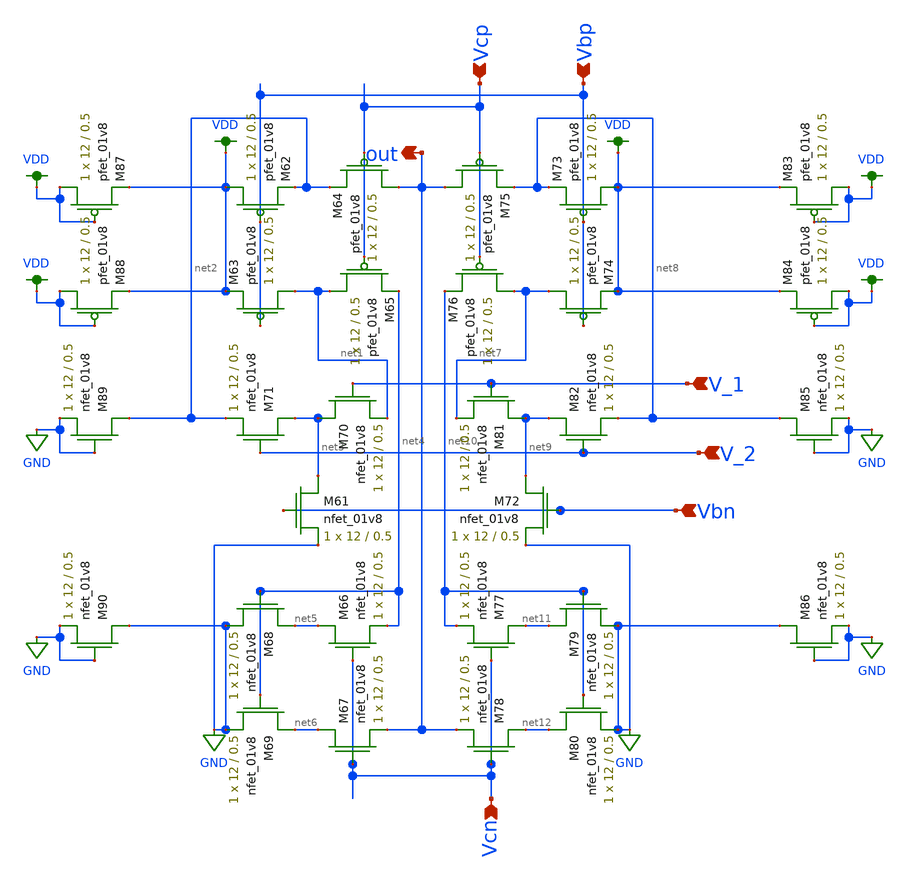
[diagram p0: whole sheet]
** sch_path: miniproject3/lfs.sch
**.subckt lfs V_1 Vcp Vcn Vbp Vbn V_2 out
*.ipin V_1
*.ipin Vcp
*.ipin Vcn
*.ipin Vbp
*.ipin Vbn
*.ipin V_2
*.opin out
XM61 net3 Vbn GND GND sky130_fd_pr__nfet_01v8 L=0.5 W=12 nf=1 ad='int((nf+1)/2) * W/nf * 0.29' as='int((nf+2)/2) * W/nf * 0.29'
+ pd='2*int((nf+1)/2) * (W/nf + 0.29)' ps='2*int((nf+2)/2) * (W/nf + 0.29)' nrd='0.29 / W' nrs='0.29 / W'
+ sa=0 sb=0 sd=0 mult=1 m=1
XM62 VDD Vbp net2 VDD sky130_fd_pr__pfet_01v8 L=0.5 W=12 nf=1 ad='int((nf+1)/2) * W/nf * 0.29' as='int((nf+2)/2) * W/nf * 0.29'
+ pd='2*int((nf+1)/2) * (W/nf + 0.29)' ps='2*int((nf+2)/2) * (W/nf + 0.29)' nrd='0.29 / W' nrs='0.29 / W'
+ sa=0 sb=0 sd=0 mult=1 m=1
XM63 net1 Vbp VDD VDD sky130_fd_pr__pfet_01v8 L=0.5 W=12 nf=1 ad='int((nf+1)/2) * W/nf * 0.29' as='int((nf+2)/2) * W/nf * 0.29'
+ pd='2*int((nf+1)/2) * (W/nf + 0.29)' ps='2*int((nf+2)/2) * (W/nf + 0.29)' nrd='0.29 / W' nrs='0.29 / W'
+ sa=0 sb=0 sd=0 mult=1 m=1
XM64 out Vcp net2 VDD sky130_fd_pr__pfet_01v8 L=0.5 W=12 nf=1 ad='int((nf+1)/2) * W/nf * 0.29' as='int((nf+2)/2) * W/nf * 0.29'
+ pd='2*int((nf+1)/2) * (W/nf + 0.29)' ps='2*int((nf+2)/2) * (W/nf + 0.29)' nrd='0.29 / W' nrs='0.29 / W'
+ sa=0 sb=0 sd=0 mult=1 m=1
XM65 net1 Vcp net4 VDD sky130_fd_pr__pfet_01v8 L=0.5 W=12 nf=1 ad='int((nf+1)/2) * W/nf * 0.29' as='int((nf+2)/2) * W/nf * 0.29'
+ pd='2*int((nf+1)/2) * (W/nf + 0.29)' ps='2*int((nf+2)/2) * (W/nf + 0.29)' nrd='0.29 / W' nrs='0.29 / W'
+ sa=0 sb=0 sd=0 mult=1 m=1
XM66 net5 Vcn net4 GND sky130_fd_pr__nfet_01v8 L=0.5 W=12 nf=1 ad='int((nf+1)/2) * W/nf * 0.29' as='int((nf+2)/2) * W/nf * 0.29'
+ pd='2*int((nf+1)/2) * (W/nf + 0.29)' ps='2*int((nf+2)/2) * (W/nf + 0.29)' nrd='0.29 / W' nrs='0.29 / W'
+ sa=0 sb=0 sd=0 mult=1 m=1
XM67 net6 Vcn out GND sky130_fd_pr__nfet_01v8 L=0.5 W=12 nf=1 ad='int((nf+1)/2) * W/nf * 0.29' as='int((nf+2)/2) * W/nf * 0.29'
+ pd='2*int((nf+1)/2) * (W/nf + 0.29)' ps='2*int((nf+2)/2) * (W/nf + 0.29)' nrd='0.29 / W' nrs='0.29 / W'
+ sa=0 sb=0 sd=0 mult=1 m=1
XM68 net5 net4 GND GND sky130_fd_pr__nfet_01v8 L=0.5 W=12 nf=1 ad='int((nf+1)/2) * W/nf * 0.29' as='int((nf+2)/2) * W/nf * 0.29'
+ pd='2*int((nf+1)/2) * (W/nf + 0.29)' ps='2*int((nf+2)/2) * (W/nf + 0.29)' nrd='0.29 / W' nrs='0.29 / W'
+ sa=0 sb=0 sd=0 mult=1 m=1
XM69 net6 net4 GND GND sky130_fd_pr__nfet_01v8 L=0.5 W=12 nf=1 ad='int((nf+1)/2) * W/nf * 0.29' as='int((nf+2)/2) * W/nf * 0.29'
+ pd='2*int((nf+1)/2) * (W/nf + 0.29)' ps='2*int((nf+2)/2) * (W/nf + 0.29)' nrd='0.29 / W' nrs='0.29 / W'
+ sa=0 sb=0 sd=0 mult=1 m=1
XM70 net3 V_1 net1 GND sky130_fd_pr__nfet_01v8 L=0.5 W=12 nf=1 ad='int((nf+1)/2) * W/nf * 0.29' as='int((nf+2)/2) * W/nf * 0.29'
+ pd='2*int((nf+1)/2) * (W/nf + 0.29)' ps='2*int((nf+2)/2) * (W/nf + 0.29)' nrd='0.29 / W' nrs='0.29 / W'
+ sa=0 sb=0 sd=0 mult=1 m=1
XM71 net3 V_2 net2 GND sky130_fd_pr__nfet_01v8 L=0.5 W=12 nf=1 ad='int((nf+1)/2) * W/nf * 0.29' as='int((nf+2)/2) * W/nf * 0.29'
+ pd='2*int((nf+1)/2) * (W/nf + 0.29)' ps='2*int((nf+2)/2) * (W/nf + 0.29)' nrd='0.29 / W' nrs='0.29 / W'
+ sa=0 sb=0 sd=0 mult=1 m=1
XM72 net9 Vbn GND GND sky130_fd_pr__nfet_01v8 L=0.5 W=12 nf=1 ad='int((nf+1)/2) * W/nf * 0.29' as='int((nf+2)/2) * W/nf * 0.29'
+ pd='2*int((nf+1)/2) * (W/nf + 0.29)' ps='2*int((nf+2)/2) * (W/nf + 0.29)' nrd='0.29 / W' nrs='0.29 / W'
+ sa=0 sb=0 sd=0 mult=1 m=1
XM73 VDD Vbp net8 VDD sky130_fd_pr__pfet_01v8 L=0.5 W=12 nf=1 ad='int((nf+1)/2) * W/nf * 0.29' as='int((nf+2)/2) * W/nf * 0.29'
+ pd='2*int((nf+1)/2) * (W/nf + 0.29)' ps='2*int((nf+2)/2) * (W/nf + 0.29)' nrd='0.29 / W' nrs='0.29 / W'
+ sa=0 sb=0 sd=0 mult=1 m=1
XM74 net7 Vbp VDD VDD sky130_fd_pr__pfet_01v8 L=0.5 W=12 nf=1 ad='int((nf+1)/2) * W/nf * 0.29' as='int((nf+2)/2) * W/nf * 0.29'
+ pd='2*int((nf+1)/2) * (W/nf + 0.29)' ps='2*int((nf+2)/2) * (W/nf + 0.29)' nrd='0.29 / W' nrs='0.29 / W'
+ sa=0 sb=0 sd=0 mult=1 m=1
XM75 out Vcp net8 VDD sky130_fd_pr__pfet_01v8 L=0.5 W=12 nf=1 ad='int((nf+1)/2) * W/nf * 0.29' as='int((nf+2)/2) * W/nf * 0.29'
+ pd='2*int((nf+1)/2) * (W/nf + 0.29)' ps='2*int((nf+2)/2) * (W/nf + 0.29)' nrd='0.29 / W' nrs='0.29 / W'
+ sa=0 sb=0 sd=0 mult=1 m=1
XM76 net7 Vcp net10 VDD sky130_fd_pr__pfet_01v8 L=0.5 W=12 nf=1 ad='int((nf+1)/2) * W/nf * 0.29' as='int((nf+2)/2) * W/nf * 0.29'
+ pd='2*int((nf+1)/2) * (W/nf + 0.29)' ps='2*int((nf+2)/2) * (W/nf + 0.29)' nrd='0.29 / W' nrs='0.29 / W'
+ sa=0 sb=0 sd=0 mult=1 m=1
XM77 net11 Vcn net10 GND sky130_fd_pr__nfet_01v8 L=0.5 W=12 nf=1 ad='int((nf+1)/2) * W/nf * 0.29' as='int((nf+2)/2) * W/nf * 0.29'
+ pd='2*int((nf+1)/2) * (W/nf + 0.29)' ps='2*int((nf+2)/2) * (W/nf + 0.29)' nrd='0.29 / W' nrs='0.29 / W'
+ sa=0 sb=0 sd=0 mult=1 m=1
XM78 net12 Vcn out GND sky130_fd_pr__nfet_01v8 L=0.5 W=12 nf=1 ad='int((nf+1)/2) * W/nf * 0.29' as='int((nf+2)/2) * W/nf * 0.29'
+ pd='2*int((nf+1)/2) * (W/nf + 0.29)' ps='2*int((nf+2)/2) * (W/nf + 0.29)' nrd='0.29 / W' nrs='0.29 / W'
+ sa=0 sb=0 sd=0 mult=1 m=1
XM79 net11 net10 GND GND sky130_fd_pr__nfet_01v8 L=0.5 W=12 nf=1 ad='int((nf+1)/2) * W/nf * 0.29' as='int((nf+2)/2) * W/nf * 0.29'
+ pd='2*int((nf+1)/2) * (W/nf + 0.29)' ps='2*int((nf+2)/2) * (W/nf + 0.29)' nrd='0.29 / W' nrs='0.29 / W'
+ sa=0 sb=0 sd=0 mult=1 m=1
XM80 net12 net10 GND GND sky130_fd_pr__nfet_01v8 L=0.5 W=12 nf=1 ad='int((nf+1)/2) * W/nf * 0.29' as='int((nf+2)/2) * W/nf * 0.29'
+ pd='2*int((nf+1)/2) * (W/nf + 0.29)' ps='2*int((nf+2)/2) * (W/nf + 0.29)' nrd='0.29 / W' nrs='0.29 / W'
+ sa=0 sb=0 sd=0 mult=1 m=1
XM81 net9 V_1 net7 GND sky130_fd_pr__nfet_01v8 L=0.5 W=12 nf=1 ad='int((nf+1)/2) * W/nf * 0.29' as='int((nf+2)/2) * W/nf * 0.29'
+ pd='2*int((nf+1)/2) * (W/nf + 0.29)' ps='2*int((nf+2)/2) * (W/nf + 0.29)' nrd='0.29 / W' nrs='0.29 / W'
+ sa=0 sb=0 sd=0 mult=1 m=1
XM82 net9 V_2 net8 GND sky130_fd_pr__nfet_01v8 L=0.5 W=12 nf=1 ad='int((nf+1)/2) * W/nf * 0.29' as='int((nf+2)/2) * W/nf * 0.29'
+ pd='2*int((nf+1)/2) * (W/nf + 0.29)' ps='2*int((nf+2)/2) * (W/nf + 0.29)' nrd='0.29 / W' nrs='0.29 / W'
+ sa=0 sb=0 sd=0 mult=1 m=1
XM83 VDD VDD VDD VDD sky130_fd_pr__pfet_01v8 L=0.5 W=12 nf=1 ad='int((nf+1)/2) * W/nf * 0.29' as='int((nf+2)/2) * W/nf * 0.29'
+ pd='2*int((nf+1)/2) * (W/nf + 0.29)' ps='2*int((nf+2)/2) * (W/nf + 0.29)' nrd='0.29 / W' nrs='0.29 / W'
+ sa=0 sb=0 sd=0 mult=1 m=1
XM84 VDD VDD VDD VDD sky130_fd_pr__pfet_01v8 L=0.5 W=12 nf=1 ad='int((nf+1)/2) * W/nf * 0.29' as='int((nf+2)/2) * W/nf * 0.29'
+ pd='2*int((nf+1)/2) * (W/nf + 0.29)' ps='2*int((nf+2)/2) * (W/nf + 0.29)' nrd='0.29 / W' nrs='0.29 / W'
+ sa=0 sb=0 sd=0 mult=1 m=1
XM85 net8 GND GND GND sky130_fd_pr__nfet_01v8 L=0.5 W=12 nf=1 ad='int((nf+1)/2) * W/nf * 0.29' as='int((nf+2)/2) * W/nf * 0.29'
+ pd='2*int((nf+1)/2) * (W/nf + 0.29)' ps='2*int((nf+2)/2) * (W/nf + 0.29)' nrd='0.29 / W' nrs='0.29 / W'
+ sa=0 sb=0 sd=0 mult=1 m=1
XM86 GND GND GND GND sky130_fd_pr__nfet_01v8 L=0.5 W=12 nf=1 ad='int((nf+1)/2) * W/nf * 0.29' as='int((nf+2)/2) * W/nf * 0.29'
+ pd='2*int((nf+1)/2) * (W/nf + 0.29)' ps='2*int((nf+2)/2) * (W/nf + 0.29)' nrd='0.29 / W' nrs='0.29 / W'
+ sa=0 sb=0 sd=0 mult=1 m=1
XM87 VDD VDD VDD VDD sky130_fd_pr__pfet_01v8 L=0.5 W=12 nf=1 ad='int((nf+1)/2) * W/nf * 0.29' as='int((nf+2)/2) * W/nf * 0.29'
+ pd='2*int((nf+1)/2) * (W/nf + 0.29)' ps='2*int((nf+2)/2) * (W/nf + 0.29)' nrd='0.29 / W' nrs='0.29 / W'
+ sa=0 sb=0 sd=0 mult=1 m=1
XM88 VDD VDD VDD VDD sky130_fd_pr__pfet_01v8 L=0.5 W=12 nf=1 ad='int((nf+1)/2) * W/nf * 0.29' as='int((nf+2)/2) * W/nf * 0.29'
+ pd='2*int((nf+1)/2) * (W/nf + 0.29)' ps='2*int((nf+2)/2) * (W/nf + 0.29)' nrd='0.29 / W' nrs='0.29 / W'
+ sa=0 sb=0 sd=0 mult=1 m=1
XM89 net2 GND GND GND sky130_fd_pr__nfet_01v8 L=0.5 W=12 nf=1 ad='int((nf+1)/2) * W/nf * 0.29' as='int((nf+2)/2) * W/nf * 0.29'
+ pd='2*int((nf+1)/2) * (W/nf + 0.29)' ps='2*int((nf+2)/2) * (W/nf + 0.29)' nrd='0.29 / W' nrs='0.29 / W'
+ sa=0 sb=0 sd=0 mult=1 m=1
XM90 GND GND GND GND sky130_fd_pr__nfet_01v8 L=0.5 W=12 nf=1 ad='int((nf+1)/2) * W/nf * 0.29' as='int((nf+2)/2) * W/nf * 0.29'
+ pd='2*int((nf+1)/2) * (W/nf + 0.29)' ps='2*int((nf+2)/2) * (W/nf + 0.29)' nrd='0.29 / W' nrs='0.29 / W'
+ sa=0 sb=0 sd=0 mult=1 m=1
**.ends
.GLOBAL VDD
.GLOBAL GND
.end
